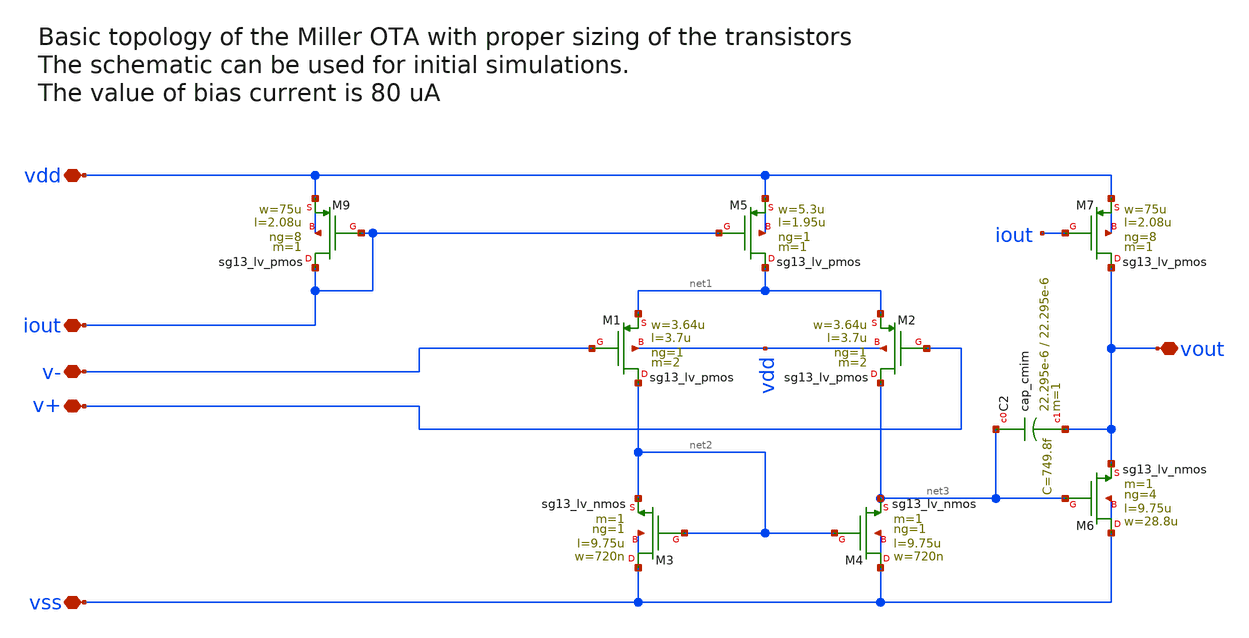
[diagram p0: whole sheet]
** sch_path: tests/data/_corecheck/OTA1336-from-main-core.sch
**.subckt OTA1336-from-main-core v- v+ vss vdd iout vout
*.iopin v-
*.iopin v+
*.iopin vss
*.iopin vdd
*.iopin iout
*.iopin vout
XM4 vss net2 net3 vss sg13_lv_nmos w=720n l=9.75u ng=1 m=1 mm_ok=1
XM3 vss net2 net2 vss sg13_lv_nmos w=720n l=9.75u ng=1 m=1 mm_ok=1
XM1 net2 v- net1 vdd sg13_lv_pmos w=3.64u l=3.7u ng=1 m=2 mm_ok=1
XM2 net3 v+ net1 vdd sg13_lv_pmos w=3.64u l=3.7u ng=1 m=2 mm_ok=1
XM5 net1 iout vdd vdd sg13_lv_pmos w=5.3u l=1.95u ng=1 m=1 mm_ok=0
XM7 vout iout vdd vdd sg13_lv_pmos w=75u l=2.08u ng=8 m=1 mm_ok=0
XM6 vss net3 vout vss sg13_lv_nmos w=28.8u l=9.75u ng=4 m=1 mm_ok=0
XM9 iout iout vdd vdd sg13_lv_pmos w=75u l=2.08u ng=8 m=1 mm_ok=0
XC2 net3 vout cap_cmim w=22.295e-6 l=22.295e-6 m=1 mm_ok=1
**.ends
.end
